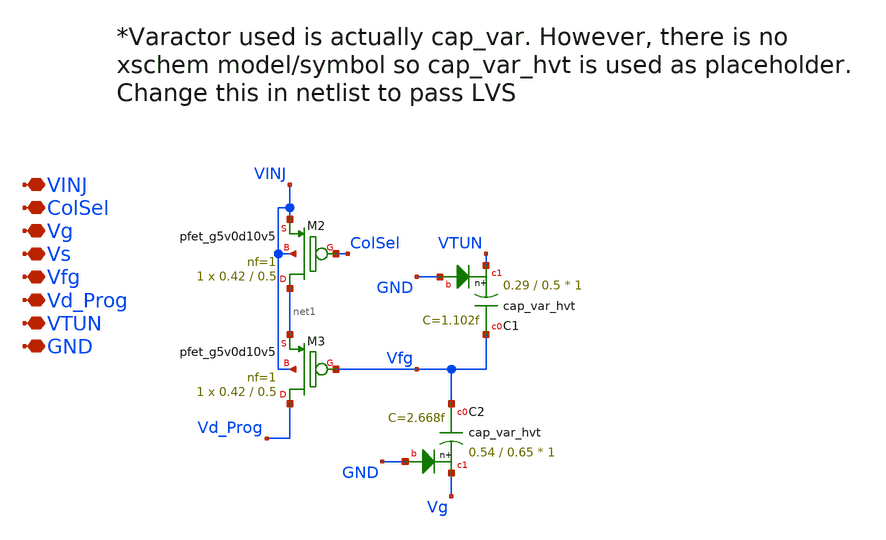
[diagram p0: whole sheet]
** sch_path: sky130_cells/Sblock/S_Block_FG_Indirect.sch
**.subckt S_Block_FG_Indirect VINJ ColSel Vg Vs Vfg Vd_Prog VTUN GND
*.iopin VINJ
*.iopin ColSel
*.iopin Vg
*.iopin Vs
*.iopin Vfg
*.iopin Vd_Prog
*.iopin VTUN
*.iopin GND
XM2 net1 ColSel VINJ VINJ sky130_fd_pr__pfet_g5v0d10v5 L=0.5 W=0.42 nf=1 ad='int((nf+1)/2) * W/nf * 0.29'
+ as='int((nf+2)/2) * W/nf * 0.29' pd='2*int((nf+1)/2) * (W/nf + 0.29)' ps='2*int((nf+2)/2) * (W/nf + 0.29)'
+ nrd='0.29 / W' nrs='0.29 / W' sa=0 sb=0 sd=0 mult=1 m=1
XM3 Vd_Prog Vfg net1 VINJ sky130_fd_pr__pfet_g5v0d10v5 L=0.5 W=0.42 nf=1 ad='int((nf+1)/2) * W/nf * 0.29'
+ as='int((nf+2)/2) * W/nf * 0.29' pd='2*int((nf+1)/2) * (W/nf + 0.29)' ps='2*int((nf+2)/2) * (W/nf + 0.29)'
+ nrd='0.29 / W' nrs='0.29 / W' sa=0 sb=0 sd=0 mult=1 m=1
XC1 Vfg VTUN GND sky130_fd_pr__cap_var_hvt W=0.29 L=0.5 VM=1 m=1
XC2 Vfg Vg GND sky130_fd_pr__cap_var_hvt W=0.54 L=0.65 VM=1 m=1
**.ends
.end
